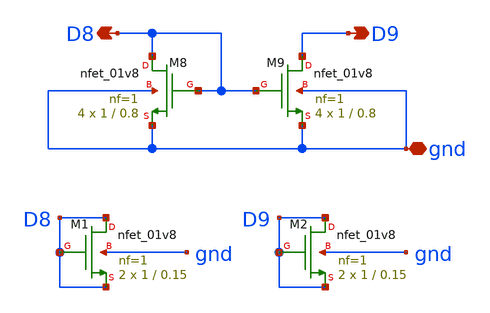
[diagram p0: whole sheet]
** sch_path: nmos_diff.sch
**.subckt nmos_diff D9 gnd D8
*.opin D9
*.iopin gnd
*.opin D8
XM8 D8 D8 gnd gnd sky130_fd_pr__nfet_01v8 L=0.8 W=1 nf=1 ad='int((nf+1)/2) * W/nf * 0.29' as='int((nf+2)/2) * W/nf * 0.29'
+ pd='2*int((nf+1)/2) * (W/nf + 0.29)' ps='2*int((nf+2)/2) * (W/nf + 0.29)' nrd='0.29 / W' nrs='0.29 / W'
+ sa=0 sb=0 sd=0 mult=4 m=4
XM9 D9 D8 gnd gnd sky130_fd_pr__nfet_01v8 L=0.8 W=1 nf=1 ad='int((nf+1)/2) * W/nf * 0.29' as='int((nf+2)/2) * W/nf * 0.29'
+ pd='2*int((nf+1)/2) * (W/nf + 0.29)' ps='2*int((nf+2)/2) * (W/nf + 0.29)' nrd='0.29 / W' nrs='0.29 / W'
+ sa=0 sb=0 sd=0 mult=4 m=4
XM2 D9 D9 D9 gnd sky130_fd_pr__nfet_01v8 L=0.15 W=1 nf=1 ad='int((nf+1)/2) * W/nf * 0.29' as='int((nf+2)/2) * W/nf * 0.29'
+ pd='2*int((nf+1)/2) * (W/nf + 0.29)' ps='2*int((nf+2)/2) * (W/nf + 0.29)' nrd='0.29 / W' nrs='0.29 / W'
+ sa=0 sb=0 sd=0 mult=2 m=2
XM1 D8 D8 D8 gnd sky130_fd_pr__nfet_01v8 L=0.15 W=1 nf=1 ad='int((nf+1)/2) * W/nf * 0.29' as='int((nf+2)/2) * W/nf * 0.29'
+ pd='2*int((nf+1)/2) * (W/nf + 0.29)' ps='2*int((nf+2)/2) * (W/nf + 0.29)' nrd='0.29 / W' nrs='0.29 / W'
+ sa=0 sb=0 sd=0 mult=2 m=2
**.ends
.end
